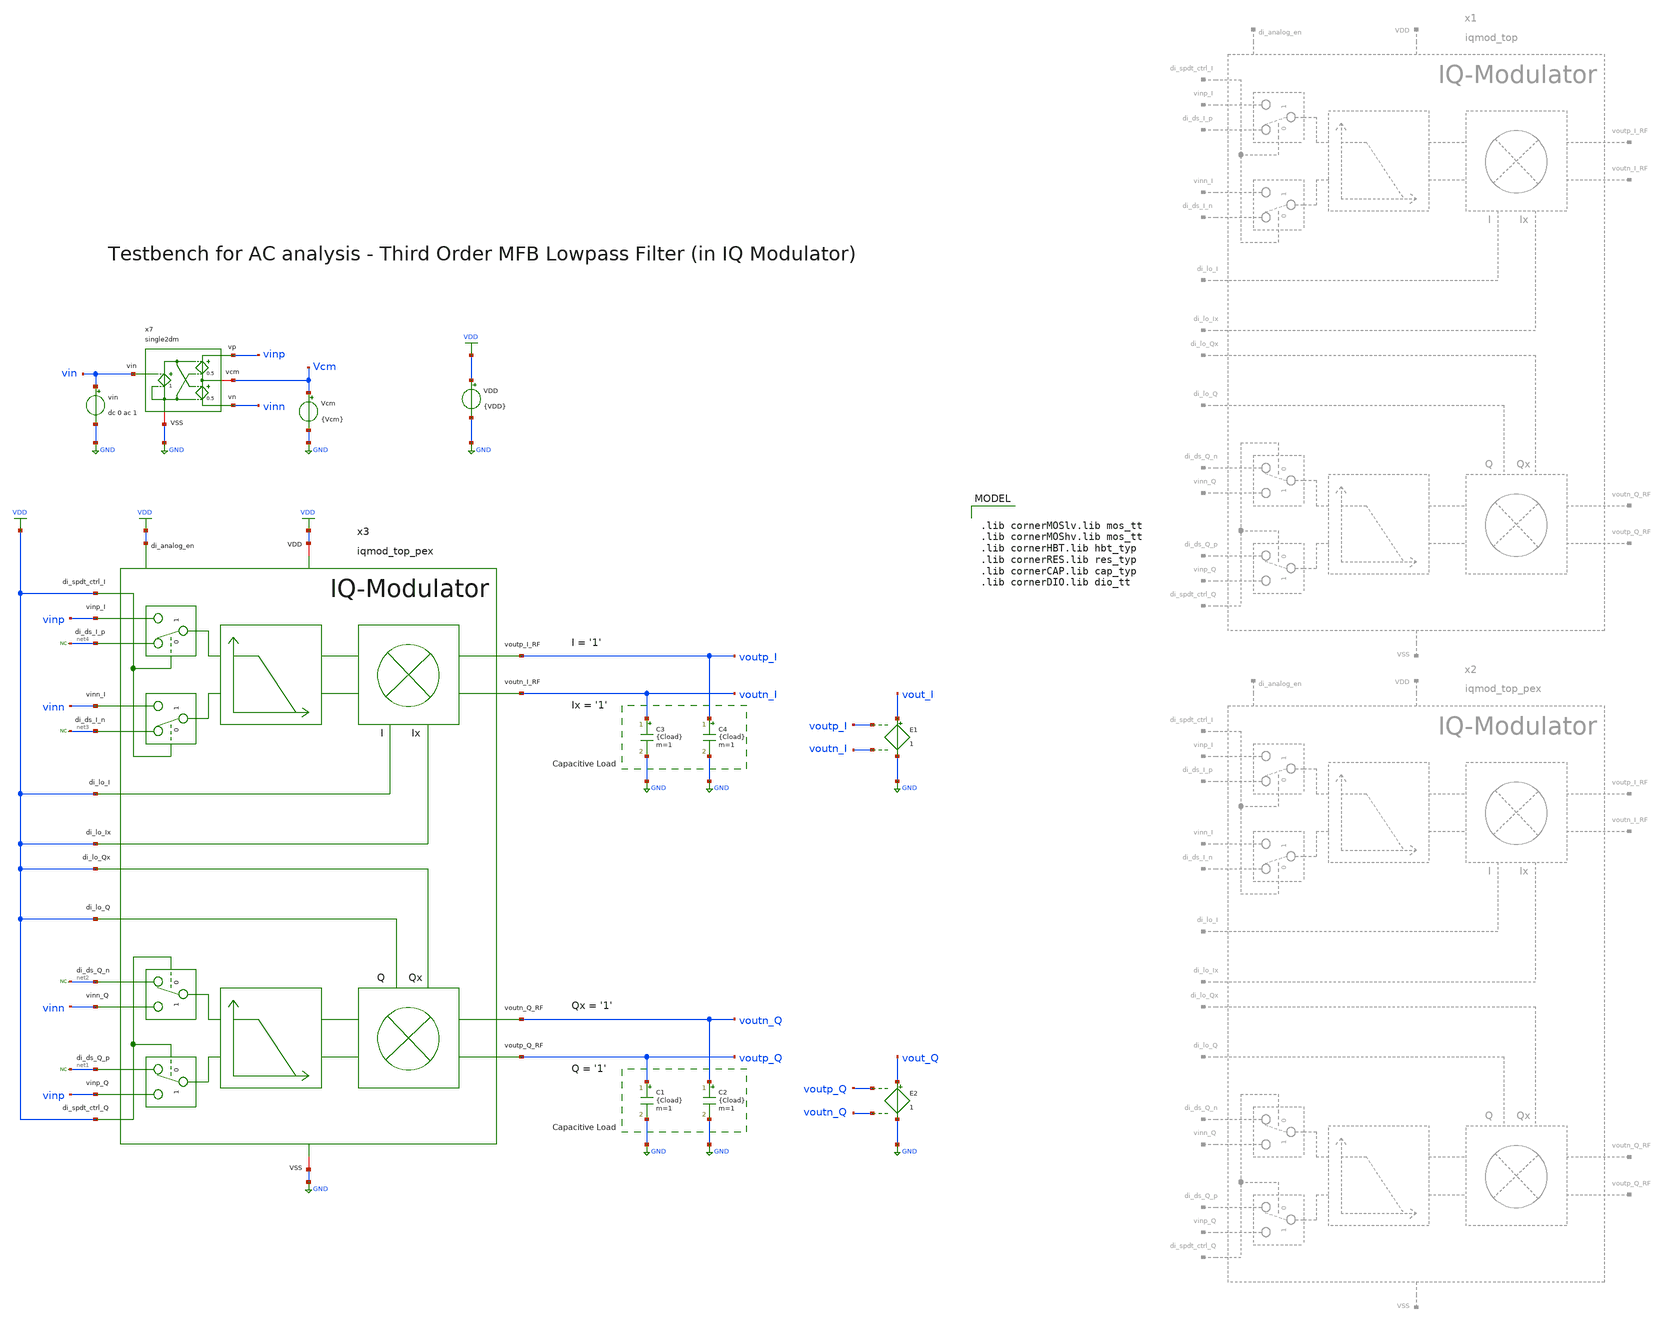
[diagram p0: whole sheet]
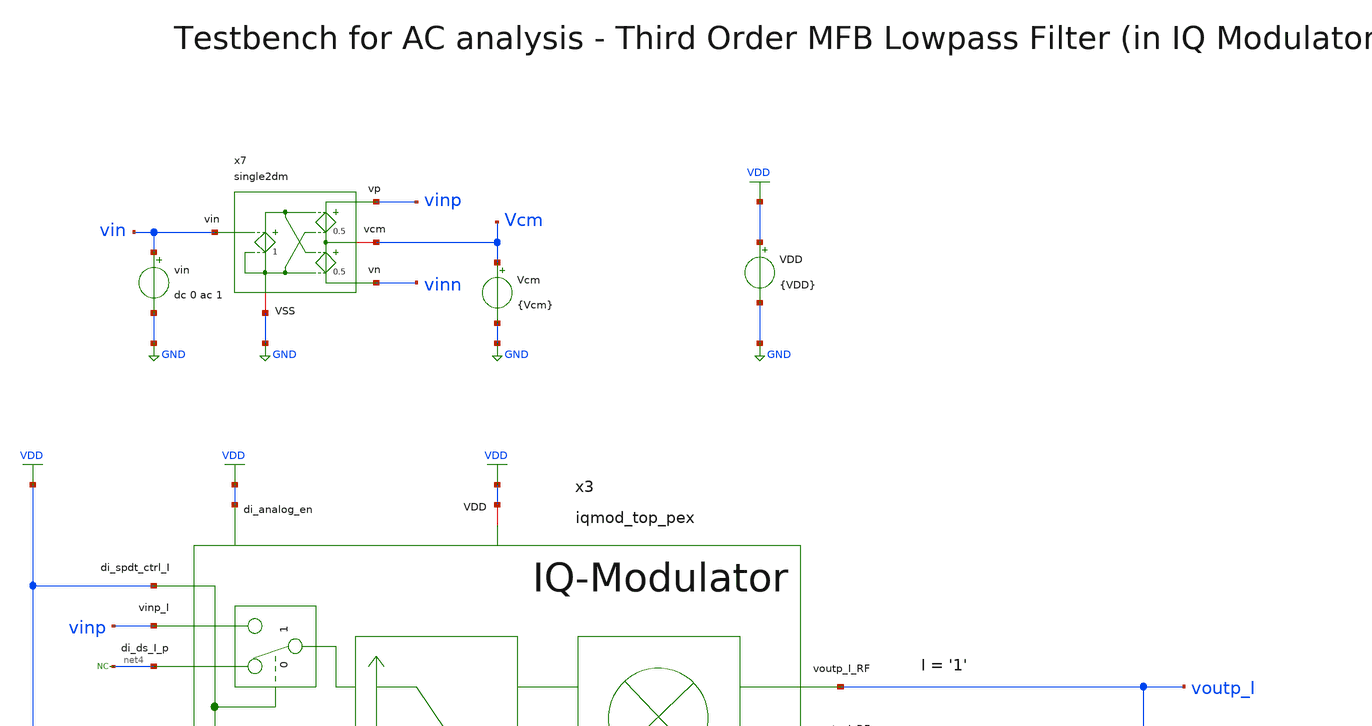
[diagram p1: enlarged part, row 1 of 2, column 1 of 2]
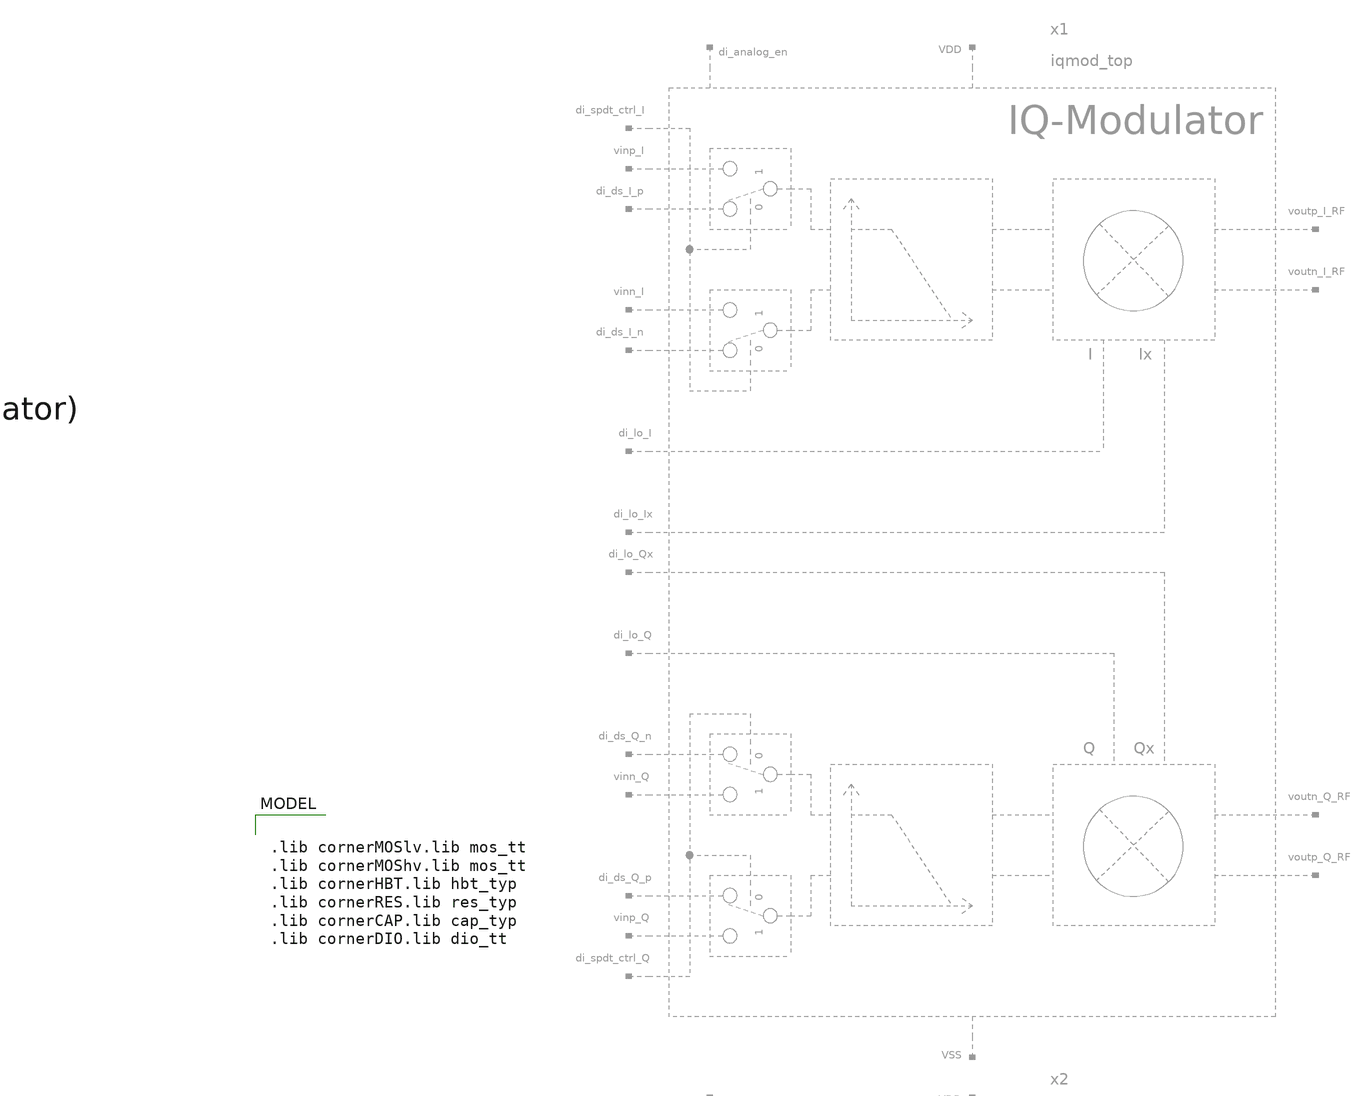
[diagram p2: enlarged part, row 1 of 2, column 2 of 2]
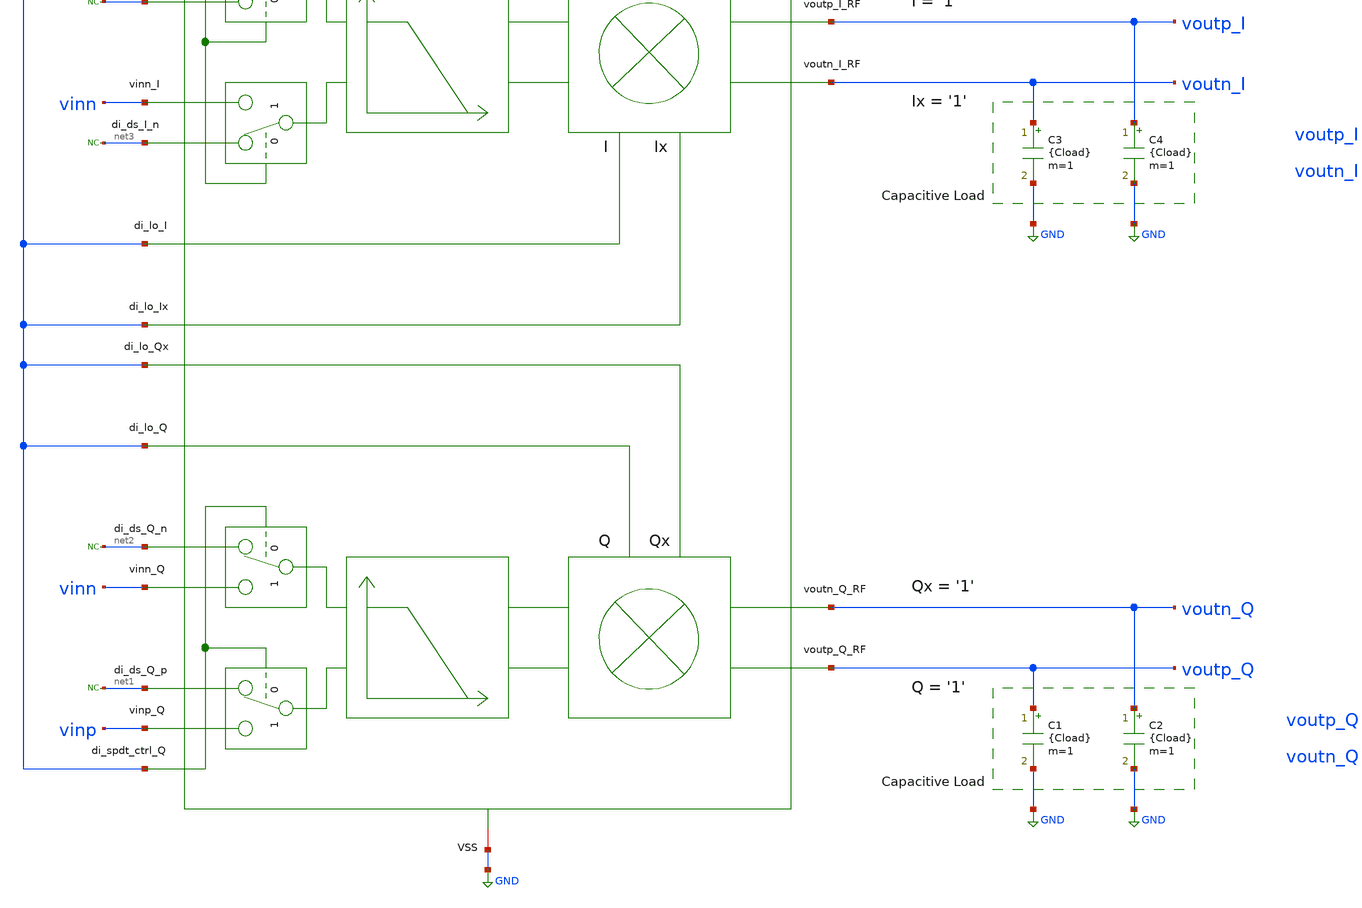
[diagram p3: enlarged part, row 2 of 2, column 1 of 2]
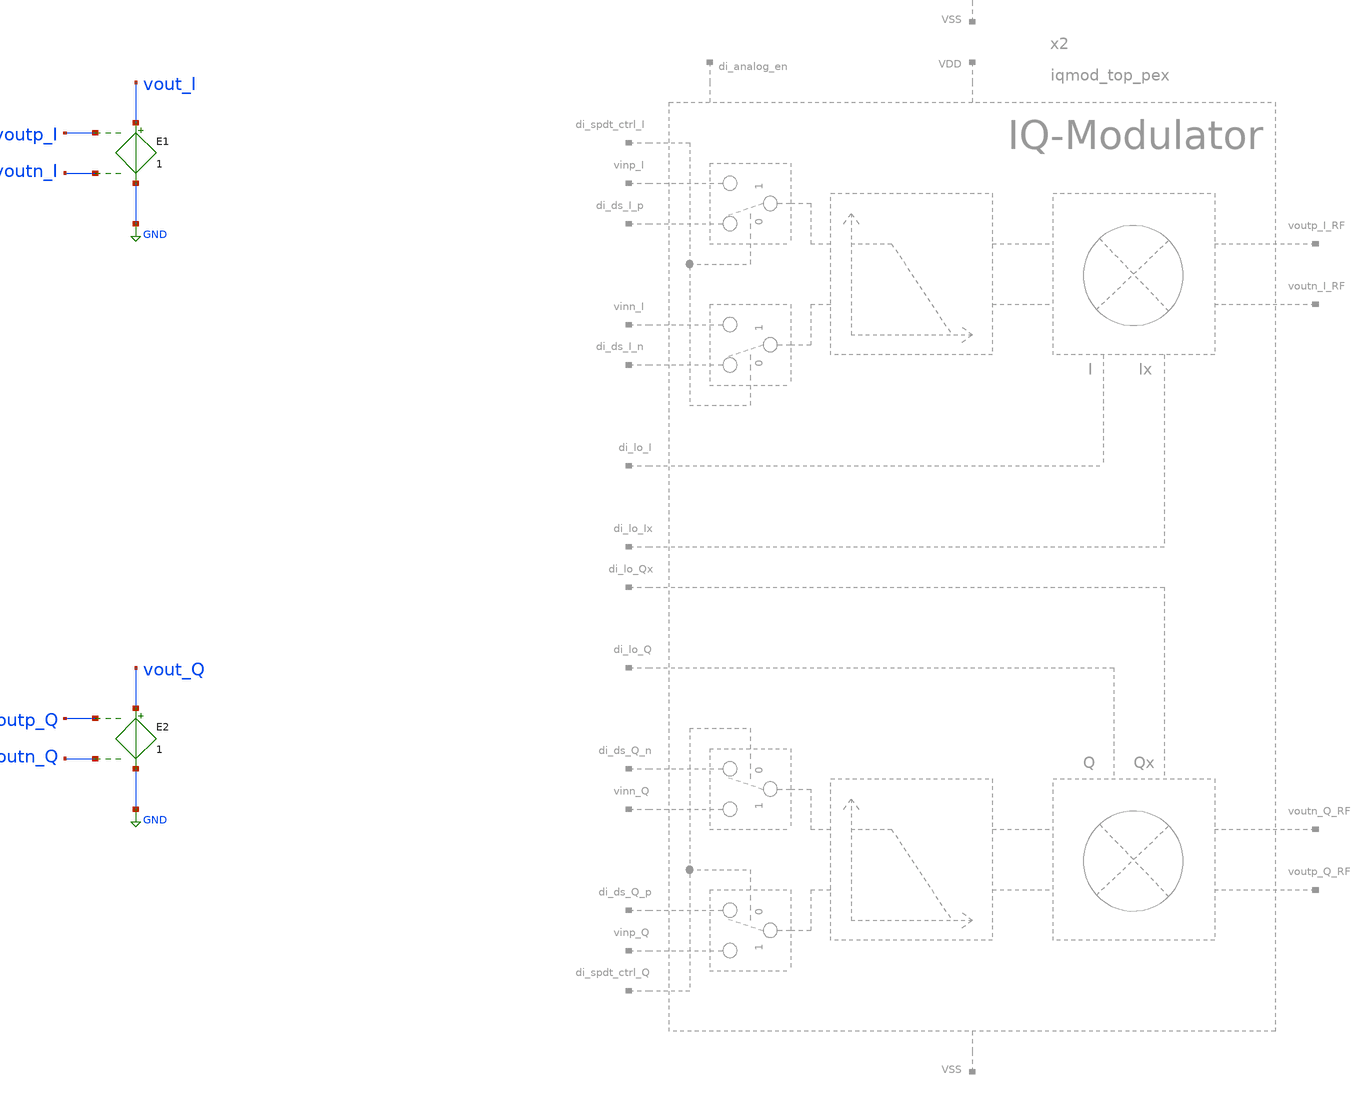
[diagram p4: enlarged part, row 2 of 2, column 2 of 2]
** sch_path: ihp130/macros/iqmod/xschem/testbenches/iqmod_top_tb_ac.sch
**.subckt iqmod_top_tb_ac
VDD VDD GND {VDD}
Vcm Vcm GND {Vcm}
vin vin GND dc 0 ac 1
x7 vinp vin Vcm GND vinn single2dm
E1 vout_I GND voutp_I voutn_I 1
E2 vout_Q GND voutp_Q voutn_Q 1
C1 voutp_Q GND {Cload} m=1
C2 voutn_Q GND {Cload} m=1
C3 voutn_I GND {Cload} m=1
C4 voutp_I GND {Cload} m=1
* noconn #net1
* noconn #net2
* noconn #net3
* noconn #net4
x3 net4 VDD net3 net2 VDD net1 vinp vinn VDD VDD voutp_I vinp vinn VDD VDD voutn_I voutp_Q voutn_Q
+ VDD GND VDD iqmod_top_pex
**** begin user architecture code


.include ../../verification/pex/iqmod_top_pex.spice
.param VDD=1.5
.param Vcm=VDD/2
.param temp=27
.param Cload=10p
.options savecurrents klu reltol=1e-3 abstol=1e-12 gmin=1e-12 rshunt=1e12
.control

save all

set wr_vecnames
set wr_singlescale

* User Constants
let f_min = 1
let f_max = 1G
let fdc = 10

* Operating Point Analysis
op
remzerovec
write iqmod_top_tb_ac.raw
set appendwrite

* AC Analysis
ac dec 101 $&const.f_min $&const.f_max
remzerovec
write iqmod_top_tb_ac.raw
set appendwrite

* Plotting
let Amag = v(vout_I)/v(vin)
let Amag_dB = vdb(Amag)
let Aarg = 180/PI*cphase(Amag)

plot Amag_dB ylabel 'Magnitude'
plot Aarg ylabel 'Phase'
plot Amag_dB Aarg ylabel 'Magnitude, Phase'

* Measurements
meas ac Adc_cl_dB find Amag_dB when frequency = fdc
print Adc_cl_dB

let Amag_fc = Adc_cl_dB-3
meas ac fcu find frequency when Amag_dB = Amag_fc FALL=1
print fcu

* Write Data
unset appendwrite
set wr_vecnames
set wr_singlescale
wrdata $PROJECT_PATH/python/plot_simulations/data/iqmod_top_tb_ac.txt v(Amag_dB) v(Aarg)

*quit
.endc



.lib cornerMOSlv.lib mos_tt
.lib cornerMOShv.lib mos_tt
.lib cornerHBT.lib hbt_typ
.lib cornerRES.lib res_typ
.lib cornerCAP.lib cap_typ
.lib cornerDIO.lib dio_tt

**** end user architecture code
**.ends
.GLOBAL GND
.GLOBAL VDD
.end
